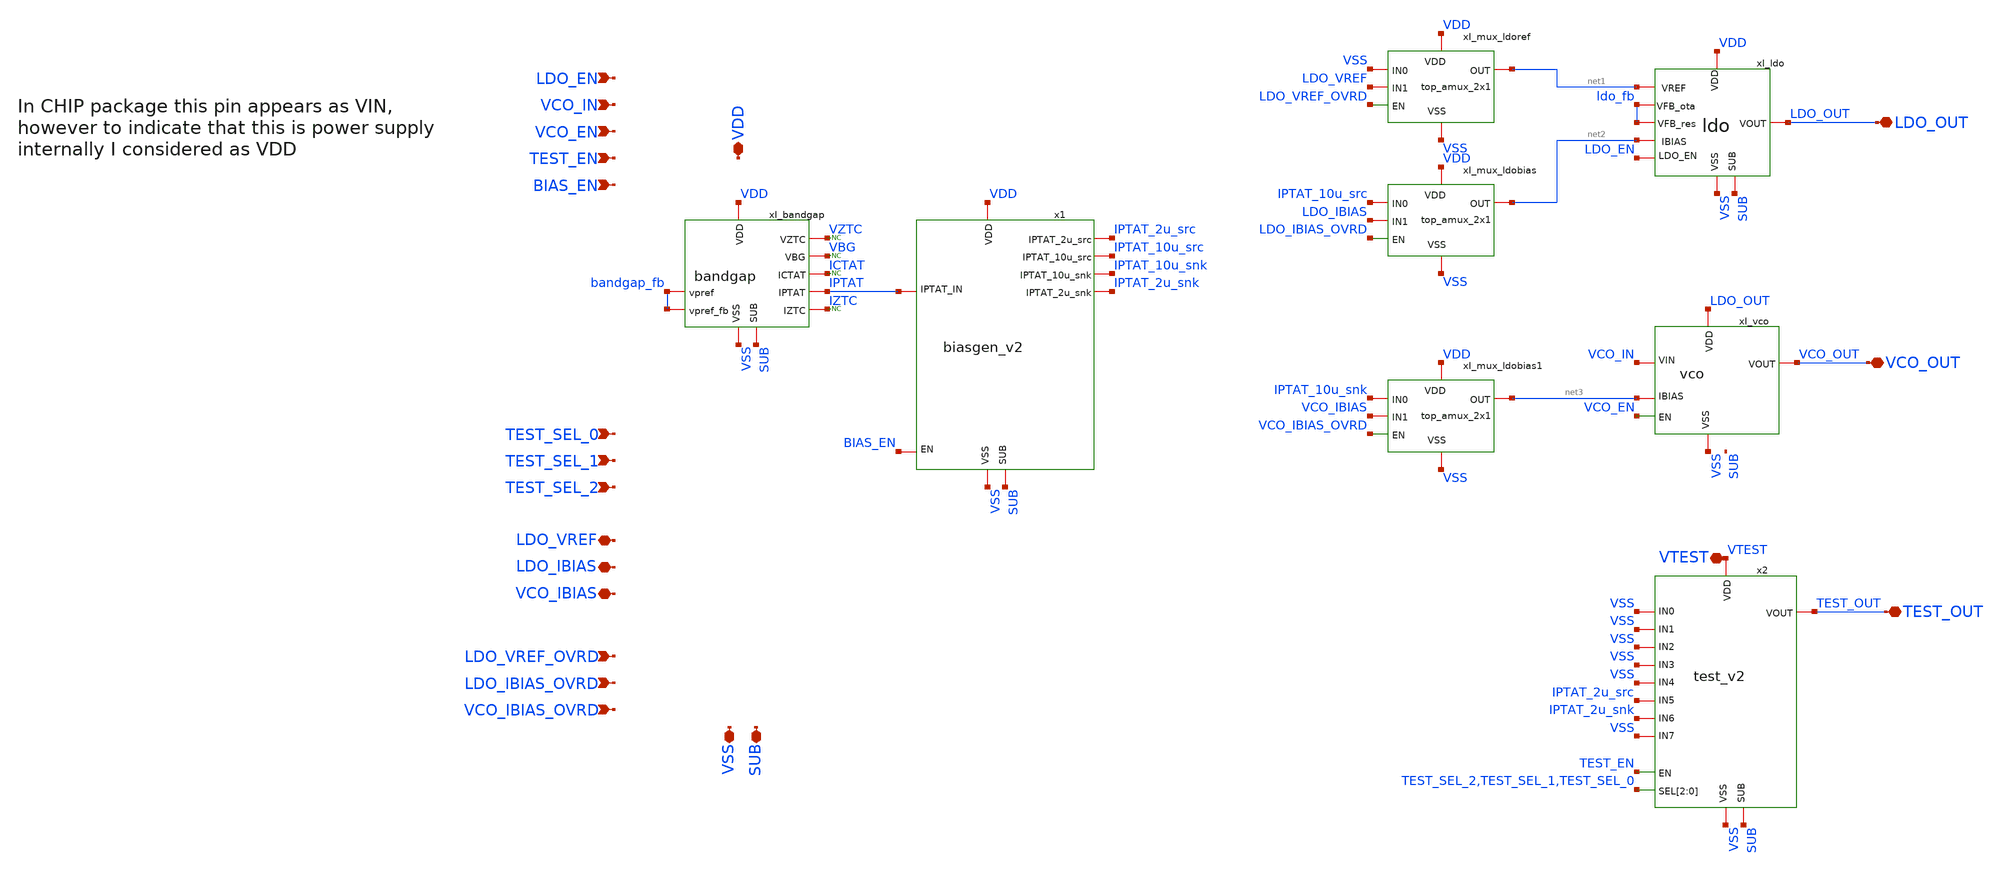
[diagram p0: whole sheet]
** sch_path: designs/libs/A1_core/A1_top_core/A1_top_core.sch
**.subckt A1_top_core TEST_SEL_0 VCO_IN VDD VSS SUB LDO_OUT VCO_OUT TEST_OUT TEST_EN VCO_EN
*+ TEST_SEL_1 TEST_SEL_2 LDO_VREF LDO_IBIAS VCO_IBIAS LDO_VREF_OVRD LDO_IBIAS_OVRD VCO_IBIAS_OVRD BIAS_EN LDO_EN
*+ VTEST
*.ipin TEST_SEL_0
*.ipin VCO_IN
*.iopin VDD
*.iopin VSS
*.iopin SUB
*.iopin LDO_OUT
*.iopin VCO_OUT
*.iopin TEST_OUT
*.ipin TEST_EN
*.ipin VCO_EN
*.ipin TEST_SEL_1
*.ipin TEST_SEL_2
*.iopin LDO_VREF
*.iopin LDO_IBIAS
*.iopin VCO_IBIAS
*.ipin LDO_VREF_OVRD
*.ipin LDO_IBIAS_OVRD
*.ipin VCO_IBIAS_OVRD
*.ipin BIAS_EN
*.ipin LDO_EN
*.iopin VTEST
xI_bandgap VDD VBG IPTAT IZTC SUB VSS bandgap_fb bandgap_fb ICTAT VZTC bandgap
xI_ldo VDD net1 LDO_OUT net2 SUB VSS LDO_EN ldo_fb ldo_fb ldo
xI_vco LDO_OUT net3 VCO_OUT VCO_EN VSS VCO_IN vco
xI_mux_ldoref VSS VDD net1 VSS LDO_VREF LDO_VREF_OVRD top_amux_2x1
xI_mux_ldobias IPTAT_10u_src VDD net2 VSS LDO_IBIAS LDO_IBIAS_OVRD top_amux_2x1
xI_mux_ldobias1 IPTAT_10u_snk VDD net3 VSS VCO_IBIAS VCO_IBIAS_OVRD top_amux_2x1
* noconn VZTC
* noconn ICTAT
* noconn VBG
* noconn IZTC
x1 VDD IPTAT_2u_src IPTAT SUB VSS IPTAT_10u_src IPTAT_10u_snk IPTAT_2u_snk BIAS_EN biasgen_v2
x2 VTEST TEST_OUT TEST_EN TEST_SEL_2 TEST_SEL_1 TEST_SEL_0 SUB VSS VSS VSS VSS VSS VSS IPTAT_2u_src
+ IPTAT_2u_snk VSS test_v2
**.ends
.end
